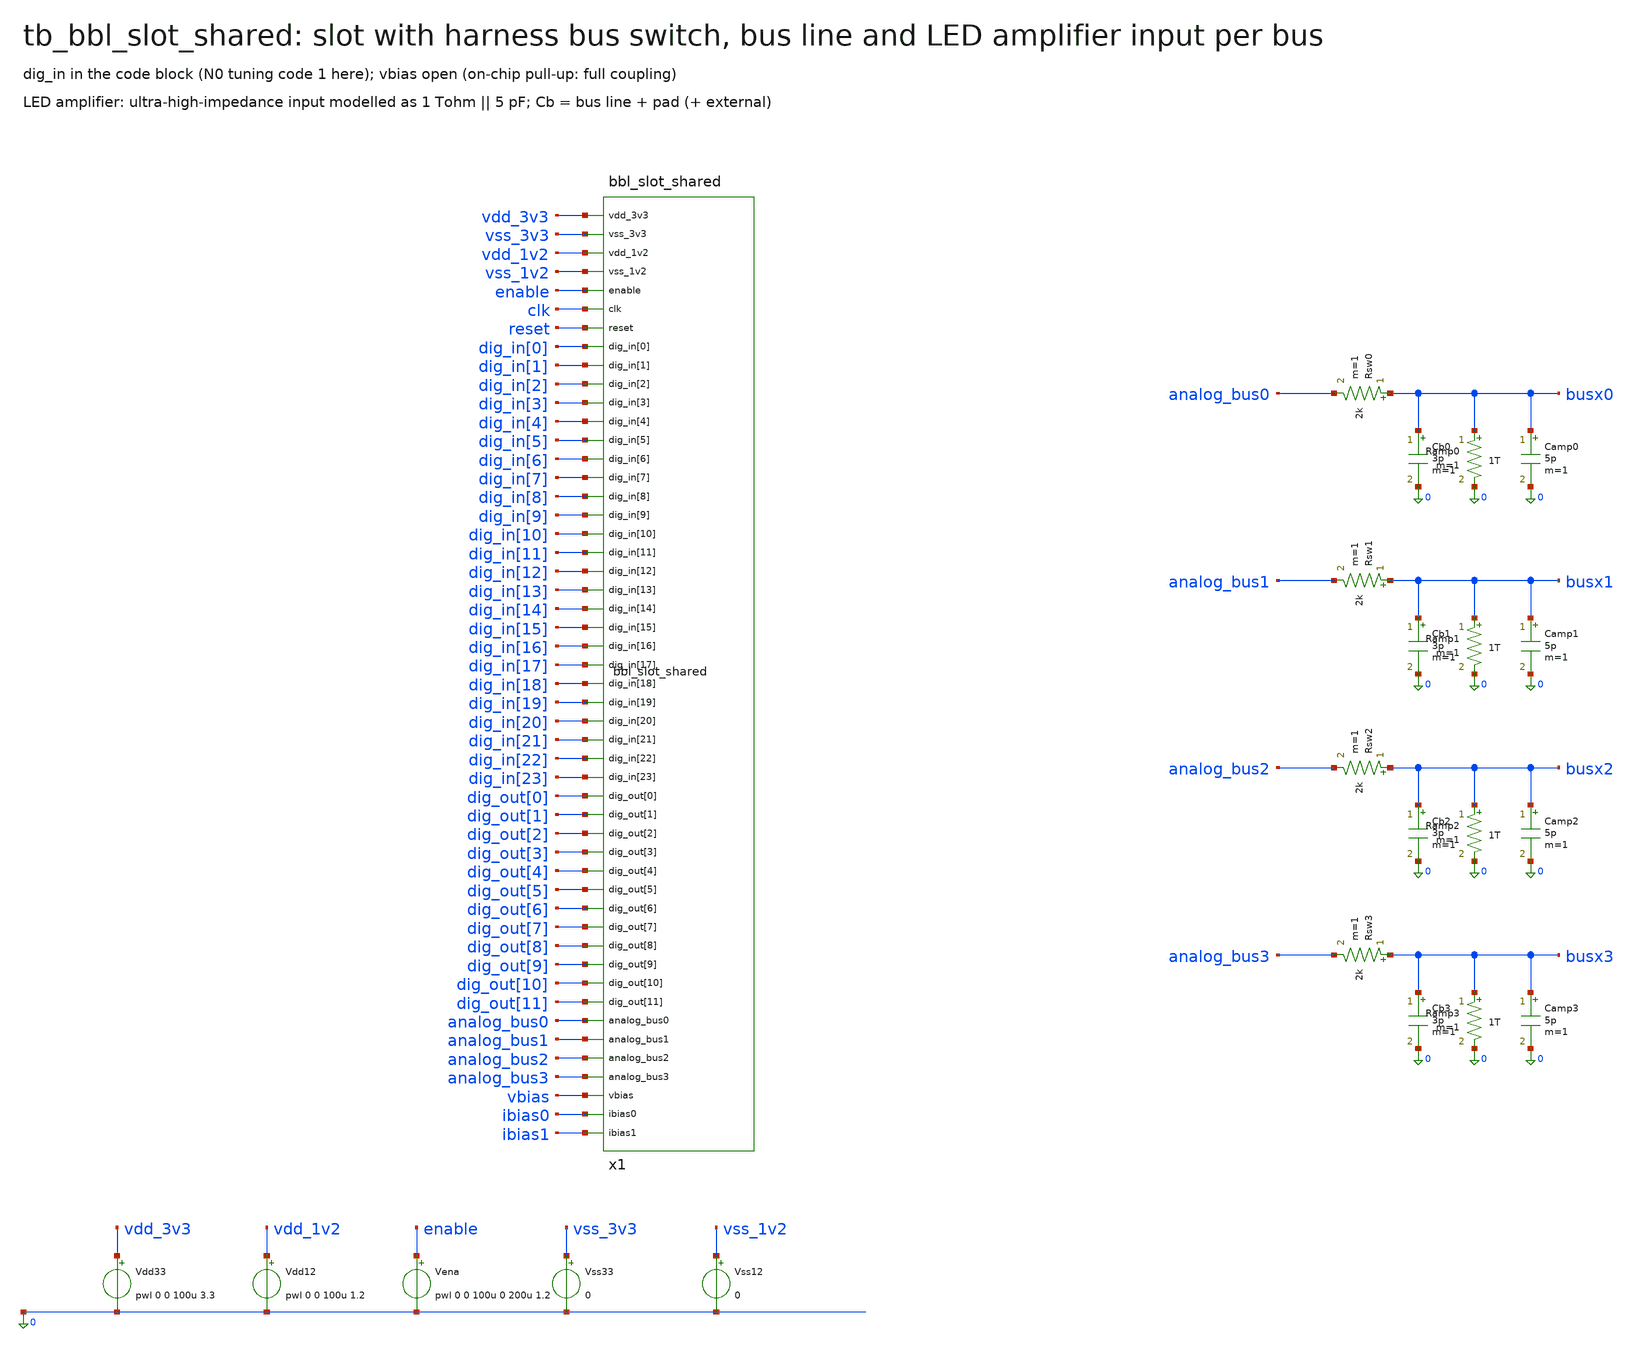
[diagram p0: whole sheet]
** sch_path: schematic/xschem/tb_bbl_slot_shared.sch
**.subckt tb_bbl_slot_shared
x1 vdd_3v3 vss_3v3 vdd_1v2 vss_1v2 enable clk reset dig_in[0] dig_in[1] dig_in[2] dig_in[3]
+ dig_in[4] dig_in[5] dig_in[6] dig_in[7] dig_in[8] dig_in[9] dig_in[10] dig_in[11] dig_in[12] dig_in[13]
+ dig_in[14] dig_in[15] dig_in[16] dig_in[17] dig_in[18] dig_in[19] dig_in[20] dig_in[21] dig_in[22] dig_in[23]
+ dig_out[0] dig_out[1] dig_out[2] dig_out[3] dig_out[4] dig_out[5] dig_out[6] dig_out[7] dig_out[8] dig_out[9]
+ dig_out[10] dig_out[11] analog_bus0 analog_bus1 analog_bus2 analog_bus3 vbias ibias0 ibias1 bbl_slot_shared
Vdd33 vdd_3v3 0 pwl 0 0 100u 3.3
Vdd12 vdd_1v2 0 pwl 0 0 100u 1.2
Vena enable 0 pwl 0 0 100u 0 200u 1.2
Vss33 vss_3v3 0 0
Vss12 vss_1v2 0 0
Rsw0 busx0 analog_bus0 2k m=1
Cb0 busx0 0 3p m=1
Ramp0 busx0 0 1T m=1
Camp0 busx0 0 5p m=1
Rsw1 busx1 analog_bus1 2k m=1
Cb1 busx1 0 3p m=1
Ramp1 busx1 0 1T m=1
Camp1 busx1 0 5p m=1
Rsw2 busx2 analog_bus2 2k m=1
Cb2 busx2 0 3p m=1
Ramp2 busx2 0 1T m=1
Camp2 busx2 0 5p m=1
Rsw3 busx3 analog_bus3 2k m=1
Cb3 busx3 0 3p m=1
Ramp3 busx3 0 1T m=1
Camp3 busx3 0 5p m=1
**** begin user architecture code

.lib cornerMOShv.lib mos_tt
.lib cornerMOSlv.lib mos_tt
.lib cornerRES.lib res_typ
.option gmin=1e-15 reltol=1e-3 abstol=1e-14 method=gear
Vd0 dig_in[0] 0 1.2
Vd1 dig_in[1] 0 0
Vd2 dig_in[2] 0 0
Vd3 dig_in[3] 0 0
Vd4 dig_in[4] 0 0
Vd5 dig_in[5] 0 0
Vd6 dig_in[6] 0 0
Vd7 dig_in[7] 0 0
Vd8 dig_in[8] 0 0
Vd9 dig_in[9] 0 0
Vd10 dig_in[10] 0 0
Vd11 dig_in[11] 0 0
Vd12 dig_in[12] 0 0
Vd13 dig_in[13] 0 0
Vd14 dig_in[14] 0 0
Vd15 dig_in[15] 0 0
Vd16 dig_in[16] 0 0
Vd17 dig_in[17] 0 0
Vd18 dig_in[18] 0 0
Vd19 dig_in[19] 0 0
Vd20 dig_in[20] 0 0
Vd21 dig_in[21] 0 0
Vd22 dig_in[22] 0 0
Vd23 dig_in[23] 0 0
.control
tran 10u 2.5
wrdata tb_bbl_slot_shared.dat v(analog_bus0) v(analog_bus1) v(analog_bus2) v(analog_bus3)
.endc


**** end user architecture code
**.ends

* expanding   symbol:  bbl_slot_shared.sym # of pins=50
** sym_path: schematic/xschem/bbl_slot_shared.sym
** sch_path: schematic/xschem/bbl_slot_shared.sch
.subckt bbl_slot_shared vdd_3v3 vss_3v3 vdd_1v2 vss_1v2 enable clk reset dig_in[0] dig_in[1]
+ dig_in[2] dig_in[3] dig_in[4] dig_in[5] dig_in[6] dig_in[7] dig_in[8] dig_in[9] dig_in[10] dig_in[11]
+ dig_in[12] dig_in[13] dig_in[14] dig_in[15] dig_in[16] dig_in[17] dig_in[18] dig_in[19] dig_in[20] dig_in[21]
+ dig_in[22] dig_in[23] dig_out[0] dig_out[1] dig_out[2] dig_out[3] dig_out[4] dig_out[5] dig_out[6] dig_out[7]
+ dig_out[8] dig_out[9] dig_out[10] dig_out[11] analog_bus0 analog_bus1 analog_bus2 analog_bus3 vbias ibias0
+ ibias1
*.iopin vdd_3v3
*.iopin vss_3v3
*.iopin vdd_1v2
*.iopin vss_1v2
*.iopin enable
*.iopin clk
*.iopin reset
*.iopin dig_in[0]
*.iopin dig_in[1]
*.iopin dig_in[2]
*.iopin dig_in[3]
*.iopin dig_in[4]
*.iopin dig_in[5]
*.iopin dig_in[6]
*.iopin dig_in[7]
*.iopin dig_in[8]
*.iopin dig_in[9]
*.iopin dig_in[10]
*.iopin dig_in[11]
*.iopin dig_in[12]
*.iopin dig_in[13]
*.iopin dig_in[14]
*.iopin dig_in[15]
*.iopin dig_in[16]
*.iopin dig_in[17]
*.iopin dig_in[18]
*.iopin dig_in[19]
*.iopin dig_in[20]
*.iopin dig_in[21]
*.iopin dig_in[22]
*.iopin dig_in[23]
*.iopin dig_out[0]
*.iopin dig_out[1]
*.iopin dig_out[2]
*.iopin dig_out[3]
*.iopin dig_out[4]
*.iopin dig_out[5]
*.iopin dig_out[6]
*.iopin dig_out[7]
*.iopin dig_out[8]
*.iopin dig_out[9]
*.iopin dig_out[10]
*.iopin dig_out[11]
*.iopin analog_bus0
*.iopin analog_bus1
*.iopin analog_bus2
*.iopin analog_bus3
*.iopin vbias
*.iopin ibias0
*.iopin ibias1
XC vdd_3v3 vss_3v3 vdd_1v2 vss_1v2 enable dig_in[0] dig_in[1] dig_in[2] dig_in[3] dig_in[4]
+ dig_in[5] dig_in[6] dig_in[7] dig_in[8] dig_in[9] dig_in[10] dig_in[11] dig_in[12] dig_in[13] dig_in[14]
+ dig_in[15] dig_in[16] dig_in[17] dig_in[18] dig_in[19] dig_in[20] dig_in[21] dig_in[22] dig_in[23] analog_bus0
+ analog_bus1 analog_bus2 analog_bus3 vbias vcplb bbl_core
XT vdd_1v2 vss_1v2 vss_3v3 dig_out[0] dig_out[1] dig_out[2] dig_out[3] dig_out[4] dig_out[5]
+ dig_out[6] dig_out[7] dig_out[8] dig_out[9] dig_out[10] dig_out[11] bbl_tielo
.ends


* expanding   symbol:  bbl_core.sym # of pins=35
** sym_path: schematic/xschem/bbl_core.sym
** sch_path: schematic/xschem/bbl_core.sch
.subckt bbl_core vdd vss vddl vssl ena d0 d1 d2 d3 d4 d5 d6 d7 d8 d9 d10 d11 d12 d13 d14 d15 d16 d17
+ d18 d19 d20 d21 d22 d23 bus0 bus1 bus2 bus3 vcpla vcplb
*.iopin vdd
*.iopin vss
*.iopin vddl
*.iopin vssl
*.iopin ena
*.iopin d0
*.iopin d1
*.iopin d2
*.iopin d3
*.iopin d4
*.iopin d5
*.iopin d6
*.iopin d7
*.iopin d8
*.iopin d9
*.iopin d10
*.iopin d11
*.iopin d12
*.iopin d13
*.iopin d14
*.iopin d15
*.iopin d16
*.iopin d17
*.iopin d18
*.iopin d19
*.iopin d20
*.iopin d21
*.iopin d22
*.iopin d23
*.iopin bus0
*.iopin bus1
*.iopin bus2
*.iopin bus3
*.iopin vcpla
*.iopin vcplb
XB vdd vss vddl vssl ena vbnl vcpla vcplb bbl_bias
XU0 vdd vss vm0 out0 vbnl d0 d1 d2 d3 bbl_unit
XU1 vdd vss vm1 out1 vbnl d4 d5 d6 d7 bbl_unit
XU2 vdd vss vm2 out2 vbnl d8 d9 d10 d11 bbl_unit
XU3 vdd vss vm3 out3 vbnl d12 d13 d14 d15 bbl_unit
XL0 vdd vss out0 bus0 bbl_inv
XL1 vdd vss out1 bus1 bbl_inv
XI0 vdd vss out0 spk0 bbl_inv
XI1 vdd vss out1 spk1 bbl_inv
XS01 vdd vss spk0 vm1 d16 d17 bbl_syn
XS10 vdd vss spk1 vm0 d18 d19 bbl_syn
XG01 vss vm0 vm1 vcpla d20 d21 bbl_gap
XG32 vss bus2 vm3 vcplb d22 d23 bbl_gap
XMP2 bus2 vcplb vm2 vss sg13_hv_nmos w=1u l=0.45u ng=1 m=1 mm_ok=1
XMP3 bus3 vcplb vm3 vss sg13_hv_nmos w=1u l=0.45u ng=1 m=1 mm_ok=1
.ends


* expanding   symbol:  bbl_tielo.sym # of pins=15
** sym_path: schematic/xschem/bbl_tielo.sym
** sch_path: schematic/xschem/bbl_tielo.sch
.subckt bbl_tielo vddl vssl vss q0 q1 q2 q3 q4 q5 q6 q7 q8 q9 q10 q11
*.iopin vddl
*.iopin vssl
*.iopin vss
*.iopin q0
*.iopin q1
*.iopin q2
*.iopin q3
*.iopin q4
*.iopin q5
*.iopin q6
*.iopin q7
*.iopin q8
*.iopin q9
*.iopin q10
*.iopin q11
XMT0 q0 vddl vssl vss sg13_lv_nmos w=0.3u l=0.5u ng=1 m=1 mm_ok=1
XMT1 q1 vddl vssl vss sg13_lv_nmos w=0.3u l=0.5u ng=1 m=1 mm_ok=1
XMT2 q2 vddl vssl vss sg13_lv_nmos w=0.3u l=0.5u ng=1 m=1 mm_ok=1
XMT3 q3 vddl vssl vss sg13_lv_nmos w=0.3u l=0.5u ng=1 m=1 mm_ok=1
XMT4 q4 vddl vssl vss sg13_lv_nmos w=0.3u l=0.5u ng=1 m=1 mm_ok=1
XMT5 q5 vddl vssl vss sg13_lv_nmos w=0.3u l=0.5u ng=1 m=1 mm_ok=1
XMT6 q6 vddl vssl vss sg13_lv_nmos w=0.3u l=0.5u ng=1 m=1 mm_ok=1
XMT7 q7 vddl vssl vss sg13_lv_nmos w=0.3u l=0.5u ng=1 m=1 mm_ok=1
XMT8 q8 vddl vssl vss sg13_lv_nmos w=0.3u l=0.5u ng=1 m=1 mm_ok=1
XMT9 q9 vddl vssl vss sg13_lv_nmos w=0.3u l=0.5u ng=1 m=1 mm_ok=1
XMT10 q10 vddl vssl vss sg13_lv_nmos w=0.3u l=0.5u ng=1 m=1 mm_ok=1
XMT11 q11 vddl vssl vss sg13_lv_nmos w=0.3u l=0.5u ng=1 m=1 mm_ok=1
.ends


* expanding   symbol:  bbl_bias.sym # of pins=8
** sym_path: schematic/xschem/bbl_bias.sym
** sch_path: schematic/xschem/bbl_bias.sch
.subckt bbl_bias vdd vss vddl vssl ena vbnl vcpla vcplb
*.iopin vdd
*.iopin vss
*.iopin vddl
*.iopin vssl
*.iopin ena
*.iopin vbnl
*.iopin vcpla
*.iopin vcplb
XMIP enab ena vddl vddl sg13_lv_pmos w=0.3u l=0.5u ng=1 m=1 mm_ok=1
XMPA vbn vbp vdd vdd sg13_hv_pmos w=2u l=2u ng=1 m=1 mm_ok=1
XMPB vbp vbp vdd vdd sg13_hv_pmos w=2u l=2u ng=1 m=1 mm_ok=1
XMSU vbn vdd vdd vdd sg13_hv_pmos w=4u l=0.45u ng=1 m=1 mm_ok=1
XMLP vbnl vbp vdd vdd sg13_hv_pmos w=0.3u l=8u ng=1 m=1 mm_ok=1
XMCA vcpla vbp vdd vdd sg13_hv_pmos w=0.3u l=22u ng=1 m=1 mm_ok=1
XMCB vcplb vbp vdd vdd sg13_hv_pmos w=0.3u l=22u ng=1 m=1 mm_ok=1
XMIN enab ena vssl vss sg13_lv_nmos w=0.3u l=0.5u ng=1 m=1 mm_ok=1
XMNA vbn vbn sa vss sg13_hv_nmos w=2u l=2u ng=1 m=1 mm_ok=1
XMNB vbp vbn rs vss sg13_hv_nmos w=16u l=2u ng=8 m=1 mm_ok=1
XMCL vbn enab vss vss sg13_hv_nmos w=1u l=0.45u ng=1 m=1 mm_ok=1
XMLD vbnl vbnl vss vss sg13_hv_nmos w=2u l=2u ng=1 m=1 mm_ok=1
XCA vss vcpla vss vss sg13_hv_nmos w=50u l=10u ng=5 m=1 mm_ok=1
XCB vss vcplb vss vss sg13_hv_nmos w=50u l=10u ng=5 m=1 mm_ok=1
XMEA sa ena vss vss sg13_hv_nmos w=1u l=0.45u ng=1 m=1 mm_ok=1
XR1 rs sb vss rhigh w=0.5e-6 l=41.055e-6 m=1 b=9 mm_ok=1
XMEB sb ena vss vss sg13_hv_nmos w=1u l=0.45u ng=1 m=1 mm_ok=1
.ends


* expanding   symbol:  bbl_unit.sym # of pins=9
** sym_path: schematic/xschem/bbl_unit.sym
** sch_path: schematic/xschem/bbl_unit.sch
.subckt bbl_unit vdd vss vm out vbnl b0 b1 b2 b3
*.iopin vdd
*.iopin vss
*.iopin vm
*.iopin out
*.iopin vbnl
*.iopin b0
*.iopin b1
*.iopin b2
*.iopin b3
XN vdd vss vm out vin bbl_neuron
XD vdd vss vin vbnl b0 b1 b2 b3 bbl_dac
.ends


* expanding   symbol:  bbl_inv.sym # of pins=4
** sym_path: schematic/xschem/bbl_inv.sym
** sch_path: schematic/xschem/bbl_inv.sch
.subckt bbl_inv vdd vss a y
*.iopin vdd
*.iopin vss
*.iopin a
*.iopin y
XMP y a vdd vdd sg13_hv_pmos w=1u l=0.45u ng=1 m=1 mm_ok=1
XMN y a vss vss sg13_hv_nmos w=1u l=0.45u ng=1 m=1 mm_ok=1
.ends


* expanding   symbol:  bbl_syn.sym # of pins=6
** sym_path: schematic/xschem/bbl_syn.sym
** sch_path: schematic/xschem/bbl_syn.sch
.subckt bbl_syn vdd vss spk post enw ens
*.iopin vdd
*.iopin vss
*.iopin spk
*.iopin post
*.iopin enw
*.iopin ens
XMPW gw spk vdd vdd sg13_hv_pmos w=0.3u l=0.45u ng=1 m=1 mm_ok=1
XMRW gw vss vdd vdd sg13_hv_pmos w=0.3u l=20u ng=1 m=1 mm_ok=1
XMSW post gw vdd vdd sg13_hv_pmos w=0.3u l=100u ng=1 m=1 mm_ok=1
XMPS gs spk vdd vdd sg13_hv_pmos w=0.3u l=0.45u ng=1 m=1 mm_ok=1
XMRS gs vss vdd vdd sg13_hv_pmos w=0.3u l=20u ng=1 m=1 mm_ok=1
XMSS post gs vdd vdd sg13_hv_pmos w=0.3u l=20u ng=1 m=1 mm_ok=1
XMNW gw enw bw vss sg13_hv_nmos w=0.3u l=0.45u ng=1 m=1 mm_ok=1
XMNS gs ens bs vss sg13_hv_nmos w=0.3u l=0.45u ng=1 m=1 mm_ok=1
XMBW bw spk vss vss sg13_hv_nmos w=0.3u l=0.45u ng=1 m=1 mm_ok=1
XMBS bs spk vss vss sg13_hv_nmos w=0.3u l=0.45u ng=1 m=1 mm_ok=1
.ends


* expanding   symbol:  bbl_gap.sym # of pins=6
** sym_path: schematic/xschem/bbl_gap.sym
** sch_path: schematic/xschem/bbl_gap.sch
.subckt bbl_gap vss a b vc enw ens
*.iopin vss
*.iopin a
*.iopin b
*.iopin vc
*.iopin enw
*.iopin ens
XMGW a vc gw vss sg13_hv_nmos w=0.3u l=10u ng=1 m=1 mm_ok=1
XMGS a vc gs vss sg13_hv_nmos w=1u l=0.45u ng=1 m=1 mm_ok=1
XMTW gw enw b vss sg13_hv_nmos w=0.3u l=0.45u ng=1 m=1 mm_ok=1
XMTS gs ens b vss sg13_hv_nmos w=1u l=0.45u ng=1 m=1 mm_ok=1
.ends


* expanding   symbol:  bbl_neuron.sym # of pins=5
** sym_path: schematic/xschem/bbl_neuron.sym
** sch_path: schematic/xschem/bbl_neuron.sch
.subckt bbl_neuron vdd vss vm out vin
*.iopin vdd
*.iopin vss
*.iopin vm
*.iopin out
*.iopin vin
XMR3 vm vin vdd vdd sg13_hv_pmos w=0.3u l=30u ng=1 m=1 mm_ok=1
XC1 vdd vm vdd vdd sg13_hv_pmos w=225u l=10u ng=18 m=1 mm_ok=1
XM3 vm out vdd vdd sg13_hv_pmos w=1u l=0.45u ng=1 m=1 mm_ok=1
XMR1 out vss vdd vdd sg13_hv_pmos w=0.3u l=20u ng=1 m=1 mm_ok=1
XM4 rst slow vdd vdd sg13_hv_pmos w=1u l=0.45u ng=1 m=1 mm_ok=1
XMR5 slow vss out vdd sg13_hv_pmos w=0.3u l=100u ng=1 m=1 mm_ok=1
XM2 vm rst vss vss sg13_hv_nmos w=2u l=0.45u ng=1 m=1 mm_ok=1
XM1 out vm vss vss sg13_hv_nmos w=1u l=1u ng=1 m=1 mm_ok=1
XMR2 rst vdd vss vss sg13_hv_nmos w=0.3u l=20u ng=1 m=1 mm_ok=1
XC2 vss slow vss vss sg13_hv_nmos w=40u l=10u ng=4 m=1 mm_ok=1
.ends


* expanding   symbol:  bbl_dac.sym # of pins=8
** sym_path: schematic/xschem/bbl_dac.sym
** sch_path: schematic/xschem/bbl_dac.sch
.subckt bbl_dac vdd vss vin vbnl b0 b1 b2 b3
*.iopin vdd
*.iopin vss
*.iopin vin
*.iopin vbnl
*.iopin b0
*.iopin b1
*.iopin b2
*.iopin b3
XMD vin vin vdd vdd sg13_hv_pmos w=3u l=3u ng=1 m=1 mm_ok=1
XMH vin vbnl vss vss sg13_hv_nmos w=0.3u l=9u ng=1 m=1 mm_ok=1
XMU0 vin vbnl s0 vss sg13_hv_nmos w=0.3u l=2u ng=1 m=1 mm_ok=1
XMU1 vin vbnl s1 vss sg13_hv_nmos w=0.6u l=2u ng=2 m=1 mm_ok=1
XMU2 vin vbnl s2 vss sg13_hv_nmos w=1.2u l=2u ng=4 m=1 mm_ok=1
XMU3 vin vbnl s3 vss sg13_hv_nmos w=2.4u l=2u ng=8 m=1 mm_ok=1
XMS0 s0 b0 vss vss sg13_hv_nmos w=0.3u l=0.45u ng=1 m=1 mm_ok=1
XMS1 s1 b1 vss vss sg13_hv_nmos w=0.6u l=0.45u ng=2 m=1 mm_ok=1
XMS2 s2 b2 vss vss sg13_hv_nmos w=1.2u l=0.45u ng=4 m=1 mm_ok=1
XMS3 s3 b3 vss vss sg13_hv_nmos w=2.4u l=0.45u ng=8 m=1 mm_ok=1
.ends

.end
